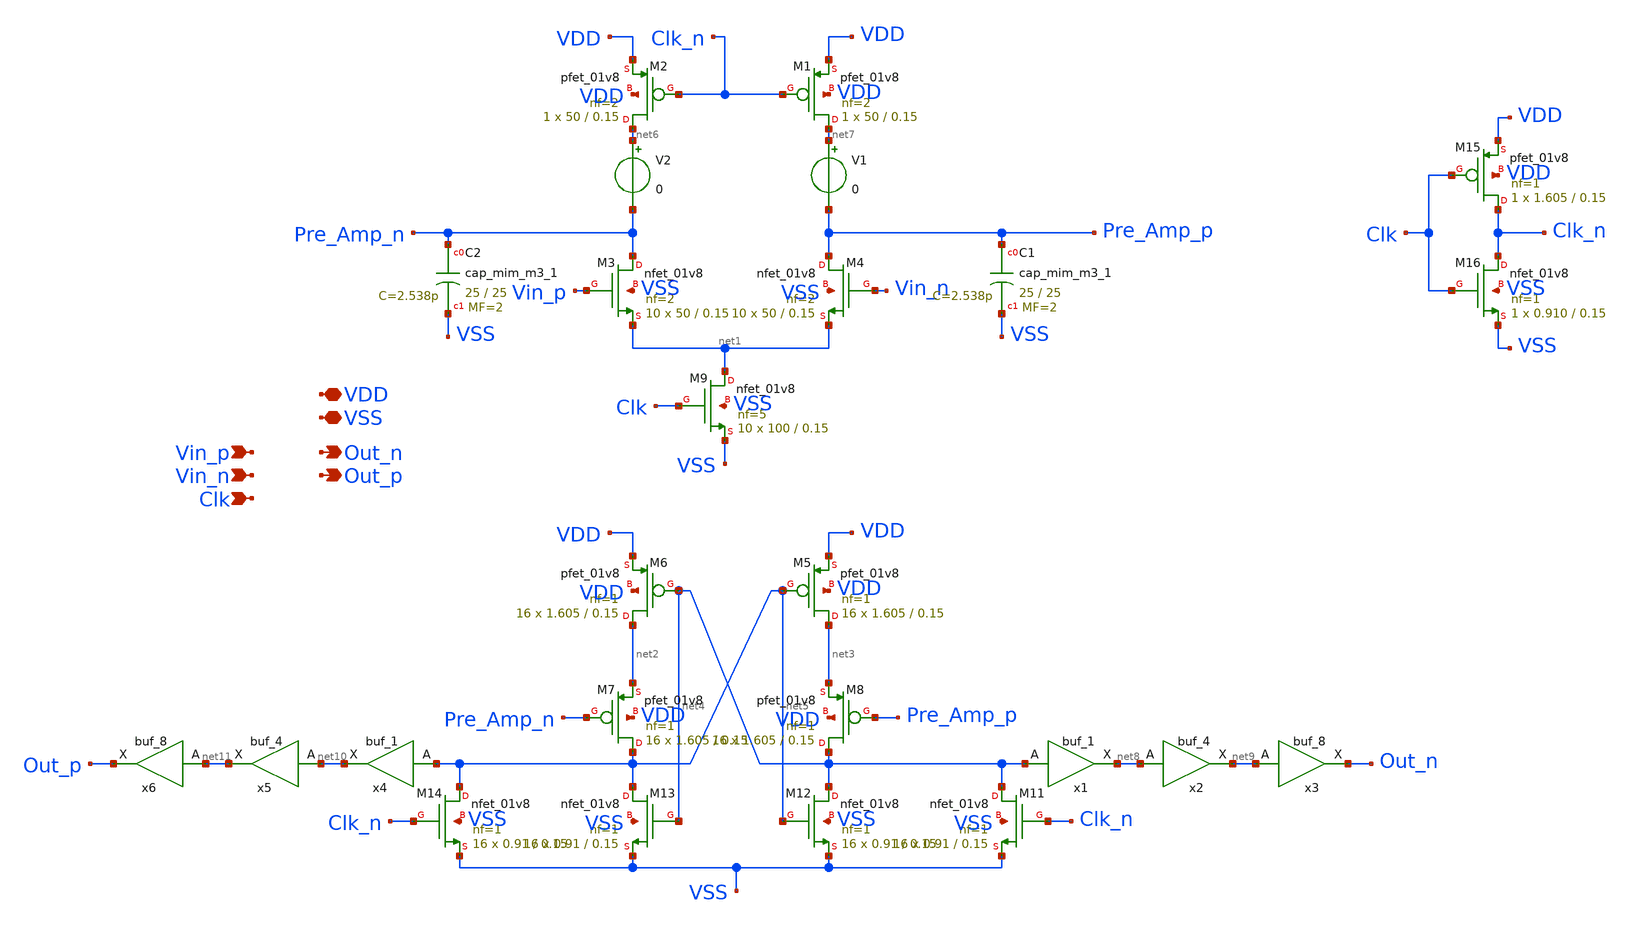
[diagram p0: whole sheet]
** sch_path: xschem/src/comparator/comparator.sch
**.subckt comparator VDD VSS Vin_p Out_n Vin_n Out_p Clk
*.iopin VDD
*.iopin VSS
*.ipin Vin_p
*.opin Out_n
*.ipin Vin_n
*.opin Out_p
*.ipin Clk
XM1 net7 Clk_n VDD VDD sky130_fd_pr__pfet_01v8 L=0.15 W=50 nf=2 ad='int((nf+1)/2) * W/nf * 0.29' as='int((nf+2)/2) * W/nf * 0.29'
+ pd='2*int((nf+1)/2) * (W/nf + 0.29)' ps='2*int((nf+2)/2) * (W/nf + 0.29)' nrd='0.29 / W' nrs='0.29 / W'
+ sa=0 sb=0 sd=0 mult=1 m=1
XM2 net6 Clk_n VDD VDD sky130_fd_pr__pfet_01v8 L=0.15 W=50 nf=2 ad='int((nf+1)/2) * W/nf * 0.29' as='int((nf+2)/2) * W/nf * 0.29'
+ pd='2*int((nf+1)/2) * (W/nf + 0.29)' ps='2*int((nf+2)/2) * (W/nf + 0.29)' nrd='0.29 / W' nrs='0.29 / W'
+ sa=0 sb=0 sd=0 mult=1 m=1
XM3 Pre_Amp_n Vin_p net1 VSS sky130_fd_pr__nfet_01v8 L=0.15 W=50 nf=2 ad='int((nf+1)/2) * W/nf * 0.29'
+ as='int((nf+2)/2) * W/nf * 0.29' pd='2*int((nf+1)/2) * (W/nf + 0.29)' ps='2*int((nf+2)/2) * (W/nf + 0.29)'
+ nrd='0.29 / W' nrs='0.29 / W' sa=0 sb=0 sd=0 mult=10 m=10
XM4 Pre_Amp_p Vin_n net1 VSS sky130_fd_pr__nfet_01v8 L=0.15 W=50 nf=2 ad='int((nf+1)/2) * W/nf * 0.29'
+ as='int((nf+2)/2) * W/nf * 0.29' pd='2*int((nf+1)/2) * (W/nf + 0.29)' ps='2*int((nf+2)/2) * (W/nf + 0.29)'
+ nrd='0.29 / W' nrs='0.29 / W' sa=0 sb=0 sd=0 mult=10 m=10
XM5 net3 net5 VDD VDD sky130_fd_pr__pfet_01v8 L=0.15 W=1.605 nf=1 ad='int((nf+1)/2) * W/nf * 0.29' as='int((nf+2)/2) * W/nf * 0.29'
+ pd='2*int((nf+1)/2) * (W/nf + 0.29)' ps='2*int((nf+2)/2) * (W/nf + 0.29)' nrd='0.29 / W' nrs='0.29 / W'
+ sa=0 sb=0 sd=0 mult=16 m=16
XM6 net2 net4 VDD VDD sky130_fd_pr__pfet_01v8 L=0.15 W=1.605 nf=1 ad='int((nf+1)/2) * W/nf * 0.29' as='int((nf+2)/2) * W/nf * 0.29'
+ pd='2*int((nf+1)/2) * (W/nf + 0.29)' ps='2*int((nf+2)/2) * (W/nf + 0.29)' nrd='0.29 / W' nrs='0.29 / W'
+ sa=0 sb=0 sd=0 mult=16 m=16
XM9 net1 Clk VSS VSS sky130_fd_pr__nfet_01v8 L=0.15 W=100 nf=5 ad='int((nf+1)/2) * W/nf * 0.29' as='int((nf+2)/2) * W/nf * 0.29'
+ pd='2*int((nf+1)/2) * (W/nf + 0.29)' ps='2*int((nf+2)/2) * (W/nf + 0.29)' nrd='0.29 / W' nrs='0.29 / W'
+ sa=0 sb=0 sd=0 mult=10 m=10
XM11 net4 Clk_n VSS VSS sky130_fd_pr__nfet_01v8 L=0.15 W=0.91 nf=1 ad='int((nf+1)/2) * W/nf * 0.29' as='int((nf+2)/2) * W/nf * 0.29'
+ pd='2*int((nf+1)/2) * (W/nf + 0.29)' ps='2*int((nf+2)/2) * (W/nf + 0.29)' nrd='0.29 / W' nrs='0.29 / W'
+ sa=0 sb=0 sd=0 mult=16 m=16
XM12 net4 net5 VSS VSS sky130_fd_pr__nfet_01v8 L=0.15 W=0.91 nf=1 ad='int((nf+1)/2) * W/nf * 0.29' as='int((nf+2)/2) * W/nf * 0.29'
+ pd='2*int((nf+1)/2) * (W/nf + 0.29)' ps='2*int((nf+2)/2) * (W/nf + 0.29)' nrd='0.29 / W' nrs='0.29 / W'
+ sa=0 sb=0 sd=0 mult=16 m=16
XM13 net5 net4 VSS VSS sky130_fd_pr__nfet_01v8 L=0.15 W=0.91 nf=1 ad='int((nf+1)/2) * W/nf * 0.29' as='int((nf+2)/2) * W/nf * 0.29'
+ pd='2*int((nf+1)/2) * (W/nf + 0.29)' ps='2*int((nf+2)/2) * (W/nf + 0.29)' nrd='0.29 / W' nrs='0.29 / W'
+ sa=0 sb=0 sd=0 mult=16 m=16
XM14 net5 Clk_n VSS VSS sky130_fd_pr__nfet_01v8 L=0.15 W=0.91 nf=1 ad='int((nf+1)/2) * W/nf * 0.29' as='int((nf+2)/2) * W/nf * 0.29'
+ pd='2*int((nf+1)/2) * (W/nf + 0.29)' ps='2*int((nf+2)/2) * (W/nf + 0.29)' nrd='0.29 / W' nrs='0.29 / W'
+ sa=0 sb=0 sd=0 mult=16 m=16
XM15 Clk_n Clk VDD VDD sky130_fd_pr__pfet_01v8 L=0.15 W=1.605 nf=1 ad='int((nf+1)/2) * W/nf * 0.29' as='int((nf+2)/2) * W/nf * 0.29'
+ pd='2*int((nf+1)/2) * (W/nf + 0.29)' ps='2*int((nf+2)/2) * (W/nf + 0.29)' nrd='0.29 / W' nrs='0.29 / W'
+ sa=0 sb=0 sd=0 mult=1 m=1
XM16 Clk_n Clk VSS VSS sky130_fd_pr__nfet_01v8 L=0.15 W=0.910 nf=1 ad='int((nf+1)/2) * W/nf * 0.29' as='int((nf+2)/2) * W/nf * 0.29'
+ pd='2*int((nf+1)/2) * (W/nf + 0.29)' ps='2*int((nf+2)/2) * (W/nf + 0.29)' nrd='0.29 / W' nrs='0.29 / W'
+ sa=0 sb=0 sd=0 mult=1 m=1
XM7 net5 Pre_Amp_n net2 VDD sky130_fd_pr__pfet_01v8 L=0.15 W=1.605 nf=1 ad='int((nf+1)/2) * W/nf * 0.29'
+ as='int((nf+2)/2) * W/nf * 0.29' pd='2*int((nf+1)/2) * (W/nf + 0.29)' ps='2*int((nf+2)/2) * (W/nf + 0.29)'
+ nrd='0.29 / W' nrs='0.29 / W' sa=0 sb=0 sd=0 mult=16 m=16
XM8 net4 Pre_Amp_p net3 VDD sky130_fd_pr__pfet_01v8 L=0.15 W=1.605 nf=1 ad='int((nf+1)/2) * W/nf * 0.29'
+ as='int((nf+2)/2) * W/nf * 0.29' pd='2*int((nf+1)/2) * (W/nf + 0.29)' ps='2*int((nf+2)/2) * (W/nf + 0.29)'
+ nrd='0.29 / W' nrs='0.29 / W' sa=0 sb=0 sd=0 mult=16 m=16
V1 net7 Pre_Amp_p 0
V2 net6 Pre_Amp_n 0
XC1 Pre_Amp_p VSS sky130_fd_pr__cap_mim_m3_1 W=25 L=25 MF=2 m=2
XC2 Pre_Amp_n VSS sky130_fd_pr__cap_mim_m3_1 W=25 L=25 MF=2 m=2
x1 net4 VSS VSS VSS VDD net8 sky130_fd_sc_hd__buf_1
x2 net8 VSS VSS VDD VDD net9 sky130_fd_sc_hd__buf_4
x3 net9 VSS VSS VDD VDD Out_n sky130_fd_sc_hd__buf_8
x4 net5 VSS VSS VSS VDD net10 sky130_fd_sc_hd__buf_1
x5 net10 VSS VSS VDD VDD net11 sky130_fd_sc_hd__buf_4
x6 net11 VSS VSS VDD VDD Out_p sky130_fd_sc_hd__buf_8
**.ends
.end
